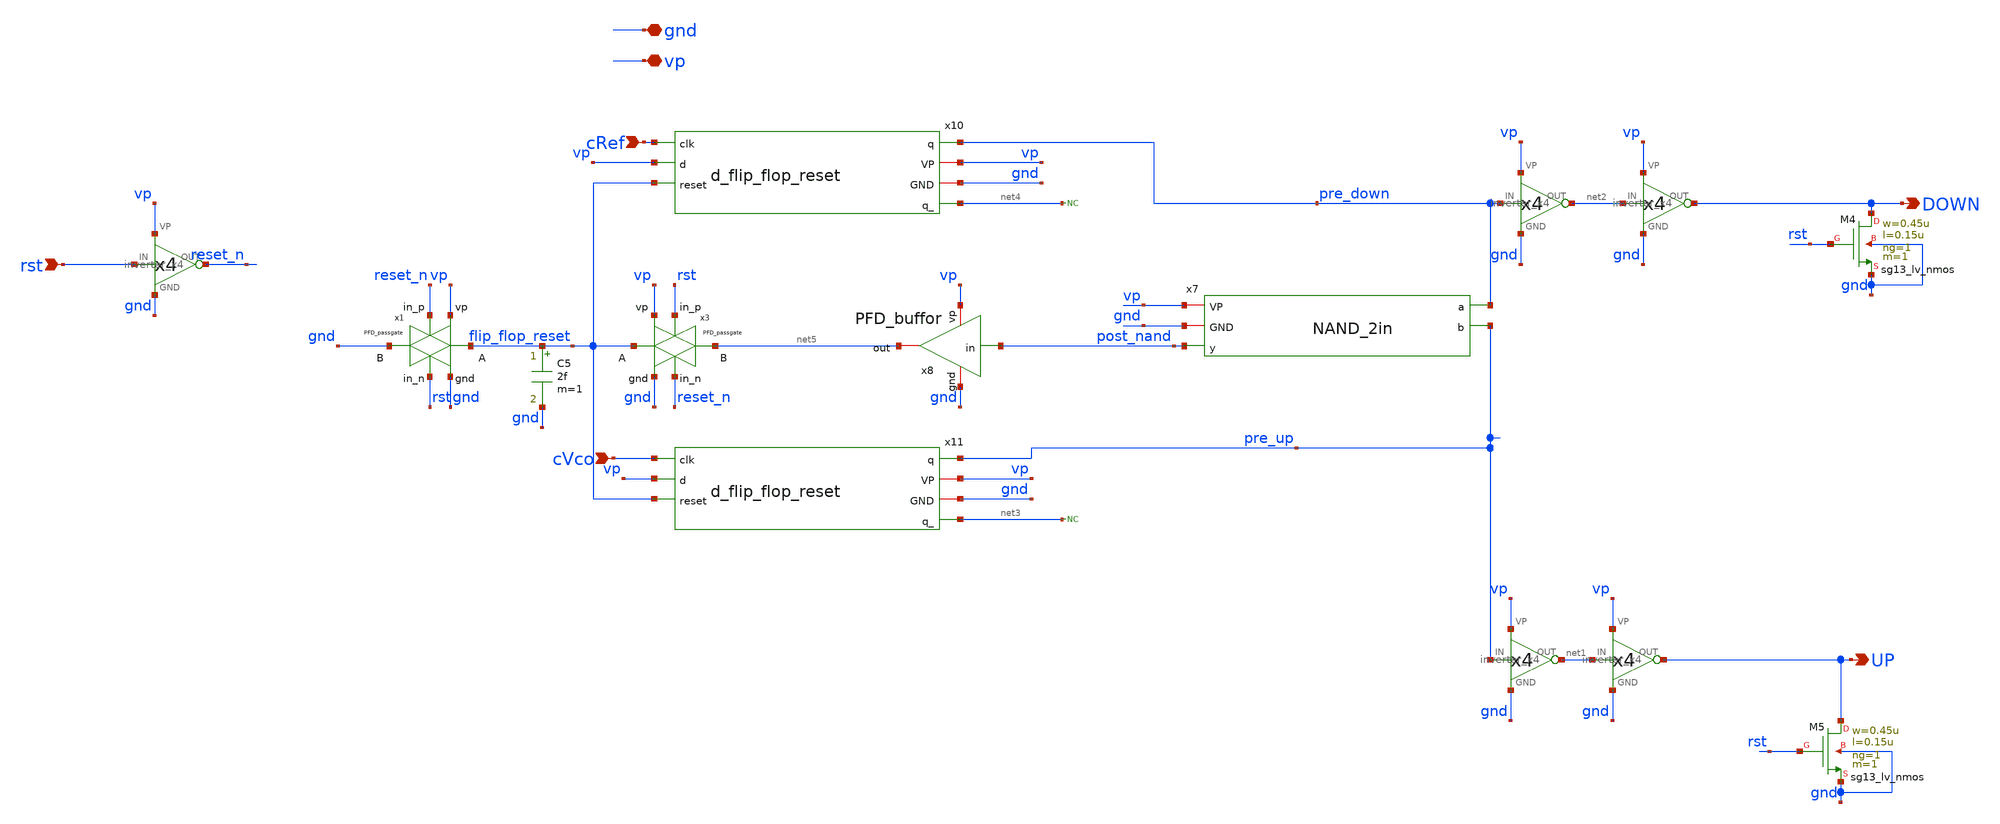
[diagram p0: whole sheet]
** sch_path: schematics/PFD/PFD_cell_2_div.sch
**.subckt PFD_cell_2_div gnd vp cRef cVco rst UP DOWN
*.iopin gnd
*.iopin vp
*.ipin cRef
*.ipin cVco
*.ipin rst
*.opin UP
*.opin DOWN
x9 rst reset_n vp gnd inverter_x4
XM4 DOWN rst gnd gnd sg13_lv_nmos w=0.45u l=0.15u ng=1 m=1 mm_ok=1
XM5 UP rst gnd gnd sg13_lv_nmos w=0.45u l=0.15u ng=1 m=1 mm_ok=1
x4 net2 DOWN vp gnd inverter_x4
x6 net1 UP vp gnd inverter_x4
x2 pre_down net2 vp gnd inverter_x4
x5 pre_up net1 vp gnd inverter_x4
x1 rst vp flip_flop_reset gnd gnd reset_n PFD_passgate
x3 reset_n vp flip_flop_reset net5 gnd rst PFD_passgate
x7 vp gnd pre_down post_nand pre_up NAND_2in
* noconn #net3
* noconn #net4
C5 flip_flop_reset gnd 2f m=1
x11 pre_up vp gnd net3 cVco vp flip_flop_reset d_flip_flop_reset
x8 gnd vp net5 post_nand PFD_buffor
x10 pre_down vp gnd net4 cRef vp flip_flop_reset d_flip_flop_reset
**.ends
.end
